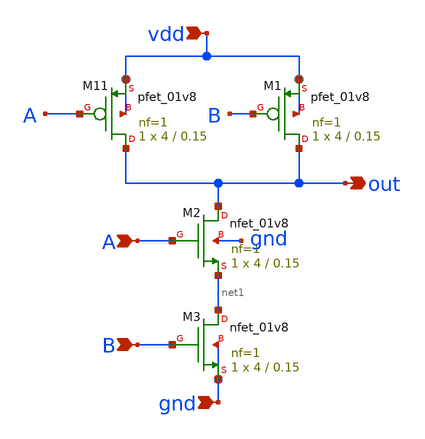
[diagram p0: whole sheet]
** sch_path: pll/dividers_lib/divider_design/nand/xschem/nand.sch
**.subckt nand vdd A B gnd out
*.ipin vdd
*.ipin A
*.ipin B
*.ipin gnd
*.opin out
XM11 out A vdd vdd sky130_fd_pr__pfet_01v8 L=0.15 W=4 nf=1 ad='int((nf+1)/2) * W/nf * 0.29' as='int((nf+2)/2) * W/nf * 0.29'
+ pd='2*int((nf+1)/2) * (W/nf + 0.29)' ps='2*int((nf+2)/2) * (W/nf + 0.29)' nrd='0.29 / W' nrs='0.29 / W'
+ sa=0 sb=0 sd=0 mult=1 m=1
XM1 out B vdd vdd sky130_fd_pr__pfet_01v8 L=0.15 W=4 nf=1 ad='int((nf+1)/2) * W/nf * 0.29' as='int((nf+2)/2) * W/nf * 0.29'
+ pd='2*int((nf+1)/2) * (W/nf + 0.29)' ps='2*int((nf+2)/2) * (W/nf + 0.29)' nrd='0.29 / W' nrs='0.29 / W'
+ sa=0 sb=0 sd=0 mult=1 m=1
XM2 out A net1 gnd sky130_fd_pr__nfet_01v8 L=0.15 W=4 nf=1 ad='int((1 + 1)/2) * 4 / 1 * 0.29' as='int((1 + 2)/2) * 4 / 1 * 0.29'
+ pd='2*int((1 + 1)/2) * (4 / 1 + 0.29)' ps='2*int((1 + 2)/2) * (4 / 1 + 0.29)' nrd='0.29 / 4 ' nrs='0.29 / 4 '
+ sa=0 sb=0 sd=0 mult=1 m=1
XM3 net1 B gnd gnd sky130_fd_pr__nfet_01v8 L=0.15 W=4 nf=1 ad='int((1 + 1)/2) * 4 / 1 * 0.29' as='int((1 + 2)/2) * 4 / 1 * 0.29'
+ pd='2*int((1 + 1)/2) * (4 / 1 + 0.29)' ps='2*int((1 + 2)/2) * (4 / 1 + 0.29)' nrd='0.29 / 4 ' nrs='0.29 / 4 '
+ sa=0 sb=0 sd=0 mult=1 m=1
**.ends
.end
